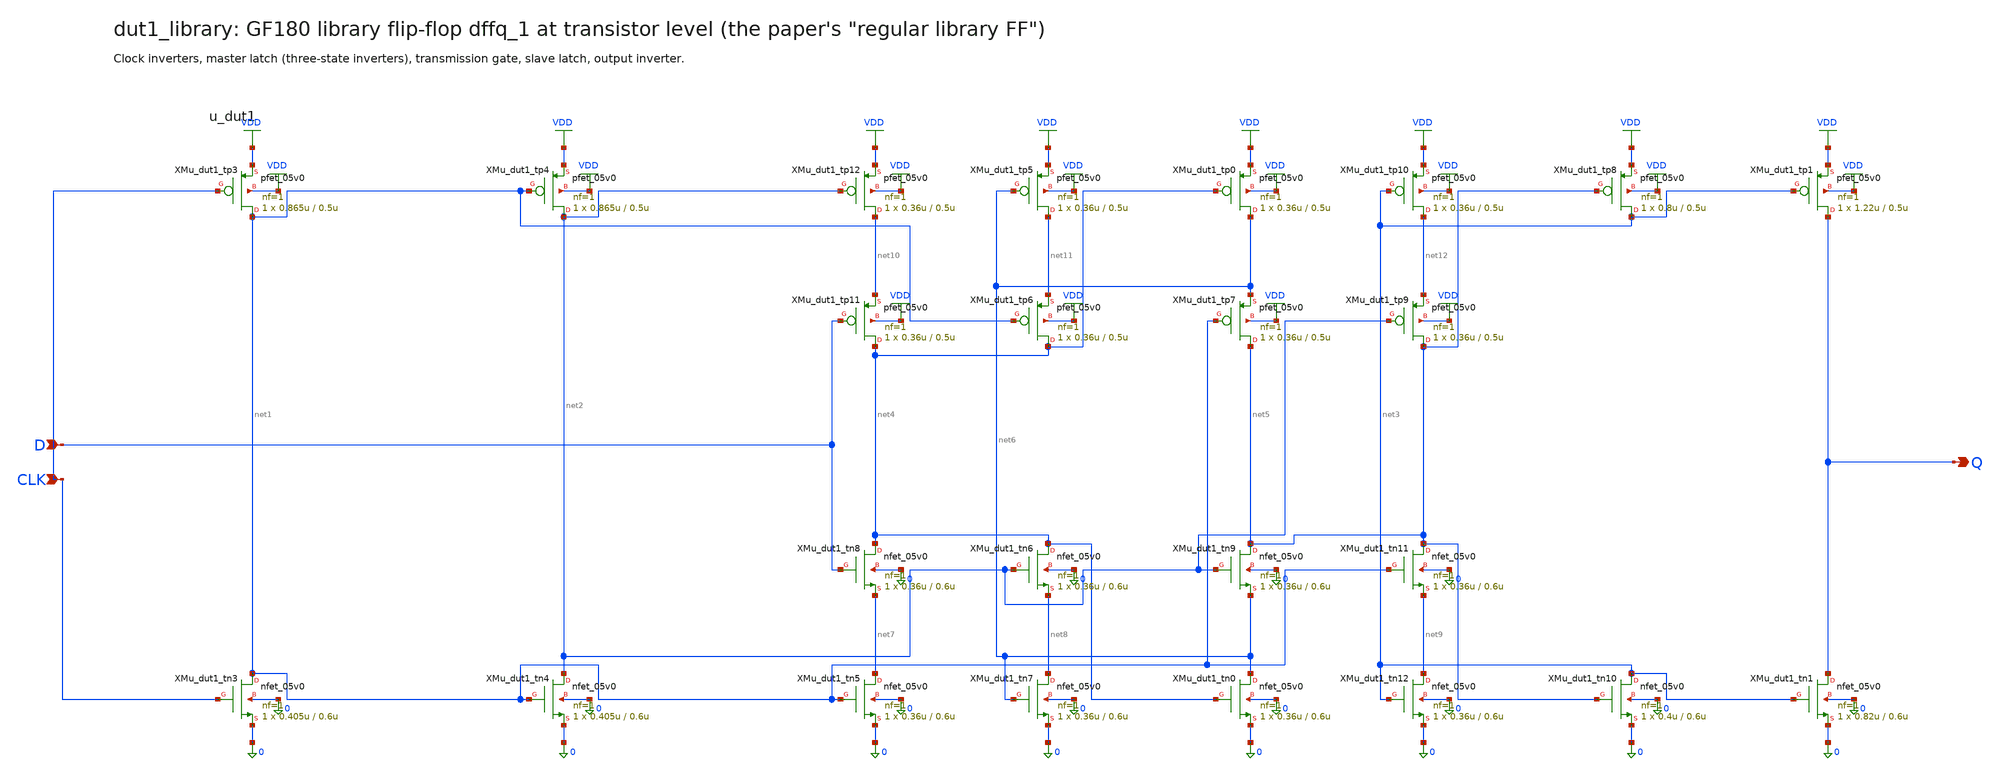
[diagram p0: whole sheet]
** sch_path: xschem/flat/dut1_library.sch
**.subckt dut1_library D CLK Q
*.ipin D
*.ipin CLK
*.opin Q
XMu_dut1_tn3 net1 CLK 0 0 nfet_05v0 L=0.6u W=0.405u nf=1 ad=2.025e-13 as=2.025e-13 pd=1.81e-06
+ ps=1.81e-06 nrd=0 nrs=0 sa=0 sb=0 sd=0 m=1
XMu_dut1_tn4 net2 net1 0 0 nfet_05v0 L=0.6u W=0.405u nf=1 ad=2.025e-13 as=2.025e-13 pd=1.81e-06
+ ps=1.81e-06 nrd=0 nrs=0 sa=0 sb=0 sd=0 m=1
XMu_dut1_tn5 net7 net1 0 0 nfet_05v0 L=0.6u W=0.36u nf=1 ad=1.8e-13 as=1.8e-13 pd=1.72e-06
+ ps=1.72e-06 nrd=0 nrs=0 sa=0 sb=0 sd=0 m=1
XMu_dut1_tn8 net4 D net7 0 nfet_05v0 L=0.6u W=0.36u nf=1 ad=1.8e-13 as=1.8e-13 pd=1.72e-06
+ ps=1.72e-06 nrd=0 nrs=0 sa=0 sb=0 sd=0 m=1
XMu_dut1_tn6 net4 net2 net8 0 nfet_05v0 L=0.6u W=0.36u nf=1 ad=1.8e-13 as=1.8e-13 pd=1.72e-06
+ ps=1.72e-06 nrd=0 nrs=0 sa=0 sb=0 sd=0 m=1
XMu_dut1_tn7 net8 net6 0 0 nfet_05v0 L=0.6u W=0.36u nf=1 ad=1.8e-13 as=1.8e-13 pd=1.72e-06
+ ps=1.72e-06 nrd=0 nrs=0 sa=0 sb=0 sd=0 m=1
XMu_dut1_tn0 net6 net4 0 0 nfet_05v0 L=0.6u W=0.36u nf=1 ad=1.8e-13 as=1.8e-13 pd=1.72e-06
+ ps=1.72e-06 nrd=0 nrs=0 sa=0 sb=0 sd=0 m=1
XMu_dut1_tn9 net5 net2 net6 0 nfet_05v0 L=0.6u W=0.36u nf=1 ad=1.8e-13 as=1.8e-13 pd=1.72e-06
+ ps=1.72e-06 nrd=0 nrs=0 sa=0 sb=0 sd=0 m=1
XMu_dut1_tn11 net5 net1 net9 0 nfet_05v0 L=0.6u W=0.36u nf=1 ad=1.8e-13 as=1.8e-13 pd=1.72e-06
+ ps=1.72e-06 nrd=0 nrs=0 sa=0 sb=0 sd=0 m=1
XMu_dut1_tn12 net9 net3 0 0 nfet_05v0 L=0.6u W=0.36u nf=1 ad=1.8e-13 as=1.8e-13 pd=1.72e-06
+ ps=1.72e-06 nrd=0 nrs=0 sa=0 sb=0 sd=0 m=1
XMu_dut1_tn10 net3 net5 0 0 nfet_05v0 L=0.6u W=0.4u nf=1 ad=2e-13 as=2e-13 pd=1.8e-06 ps=1.8e-06
+ nrd=0 nrs=0 sa=0 sb=0 sd=0 m=1
XMu_dut1_tn1 Q net3 0 0 nfet_05v0 L=0.6u W=0.82u nf=1 ad=4.1e-13 as=4.1e-13 pd=2.64e-06 ps=2.64e-06
+ nrd=0 nrs=0 sa=0 sb=0 sd=0 m=1
XMu_dut1_tp3 net1 CLK VDD VDD pfet_05v0 L=0.5u W=0.865u nf=1 ad=4.325e-13 as=4.325e-13 pd=2.73e-06
+ ps=2.73e-06 nrd=0 nrs=0 sa=0 sb=0 sd=0 m=1
XMu_dut1_tp4 net2 net1 VDD VDD pfet_05v0 L=0.5u W=0.865u nf=1 ad=4.325e-13 as=4.325e-13 pd=2.73e-06
+ ps=2.73e-06 nrd=0 nrs=0 sa=0 sb=0 sd=0 m=1
XMu_dut1_tp12 net10 net2 VDD VDD pfet_05v0 L=0.5u W=0.36u nf=1 ad=1.8e-13 as=1.8e-13 pd=1.72e-06
+ ps=1.72e-06 nrd=0 nrs=0 sa=0 sb=0 sd=0 m=1
XMu_dut1_tp11 net4 D net10 VDD pfet_05v0 L=0.5u W=0.36u nf=1 ad=1.8e-13 as=1.8e-13 pd=1.72e-06
+ ps=1.72e-06 nrd=0 nrs=0 sa=0 sb=0 sd=0 m=1
XMu_dut1_tp6 net4 net1 net11 VDD pfet_05v0 L=0.5u W=0.36u nf=1 ad=1.8e-13 as=1.8e-13 pd=1.72e-06
+ ps=1.72e-06 nrd=0 nrs=0 sa=0 sb=0 sd=0 m=1
XMu_dut1_tp5 net11 net6 VDD VDD pfet_05v0 L=0.5u W=0.36u nf=1 ad=1.8e-13 as=1.8e-13 pd=1.72e-06
+ ps=1.72e-06 nrd=0 nrs=0 sa=0 sb=0 sd=0 m=1
XMu_dut1_tp0 net6 net4 VDD VDD pfet_05v0 L=0.5u W=0.36u nf=1 ad=1.8e-13 as=1.8e-13 pd=1.72e-06
+ ps=1.72e-06 nrd=0 nrs=0 sa=0 sb=0 sd=0 m=1
XMu_dut1_tp7 net5 net1 net6 VDD pfet_05v0 L=0.5u W=0.36u nf=1 ad=1.8e-13 as=1.8e-13 pd=1.72e-06
+ ps=1.72e-06 nrd=0 nrs=0 sa=0 sb=0 sd=0 m=1
XMu_dut1_tp9 net5 net2 net12 VDD pfet_05v0 L=0.5u W=0.36u nf=1 ad=1.8e-13 as=1.8e-13 pd=1.72e-06
+ ps=1.72e-06 nrd=0 nrs=0 sa=0 sb=0 sd=0 m=1
XMu_dut1_tp10 net12 net3 VDD VDD pfet_05v0 L=0.5u W=0.36u nf=1 ad=1.8e-13 as=1.8e-13 pd=1.72e-06
+ ps=1.72e-06 nrd=0 nrs=0 sa=0 sb=0 sd=0 m=1
XMu_dut1_tp8 net3 net5 VDD VDD pfet_05v0 L=0.5u W=0.8u nf=1 ad=4e-13 as=4e-13 pd=2.6e-06 ps=2.6e-06
+ nrd=0 nrs=0 sa=0 sb=0 sd=0 m=1
XMu_dut1_tp1 Q net3 VDD VDD pfet_05v0 L=0.5u W=1.22u nf=1 ad=6.1e-13 as=6.1e-13 pd=3.44e-06
+ ps=3.44e-06 nrd=0 nrs=0 sa=0 sb=0 sd=0 m=1
**.ends
.GLOBAL VDD
.end
